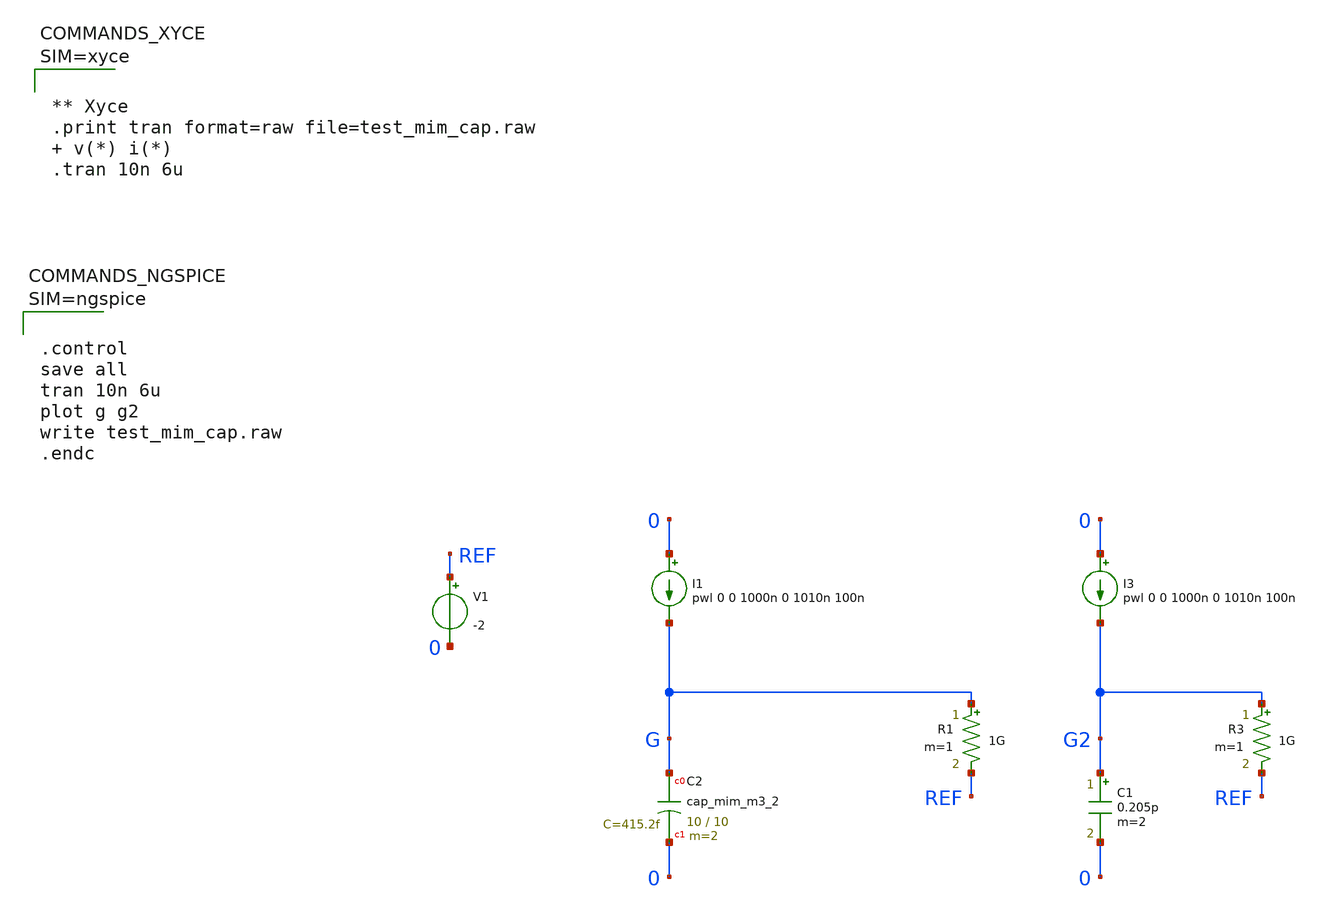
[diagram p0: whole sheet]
** sch_path: sky130A/xschem_libs/sky130_tests/test_mim_cap/schematic/test_mim_cap.sch
* Copyright 2021 Stefan Frederik Schippers
* Licensed under the Apache License, Version 2.0 (the "License");
* you may not use this file except in compliance with the License.
* You may obtain a copy of the License at
* https://www.apache.org/licenses/LICENSE-2.0
* Unless required by applicable law or agreed to in writing, software
* distributed under the License is distributed on an "AS IS" BASIS,
* WITHOUT WARRANTIES OR CONDITIONS OF ANY KIND, either express or implied.
* See the License for the specific language governing permissions and
* limitations under the License.
**.subckt test_mim_cap
I1 0 G pwl 0 0 1000n 0 1010n 100n
R1 G REF 1G m=1
I3 0 G2 pwl 0 0 1000n 0 1010n 100n
R3 G2 REF 1G m=1
C1 G2 0 0.205p m=2
V1 REF 0 -2
XC2 G 0 sky130_fd_pr__cap_mim_m3_2 W=10 L=10 MF=2 m=2
**** begin user architecture code

** opencircuitdesign pdks install
.lib $::SKYWATER_MODELS/sky130.lib.spice tt







.control
save all
tran 10n 6u
plot g g2
write test_mim_cap.raw
.endc



**** end user architecture code
**.ends
.end
